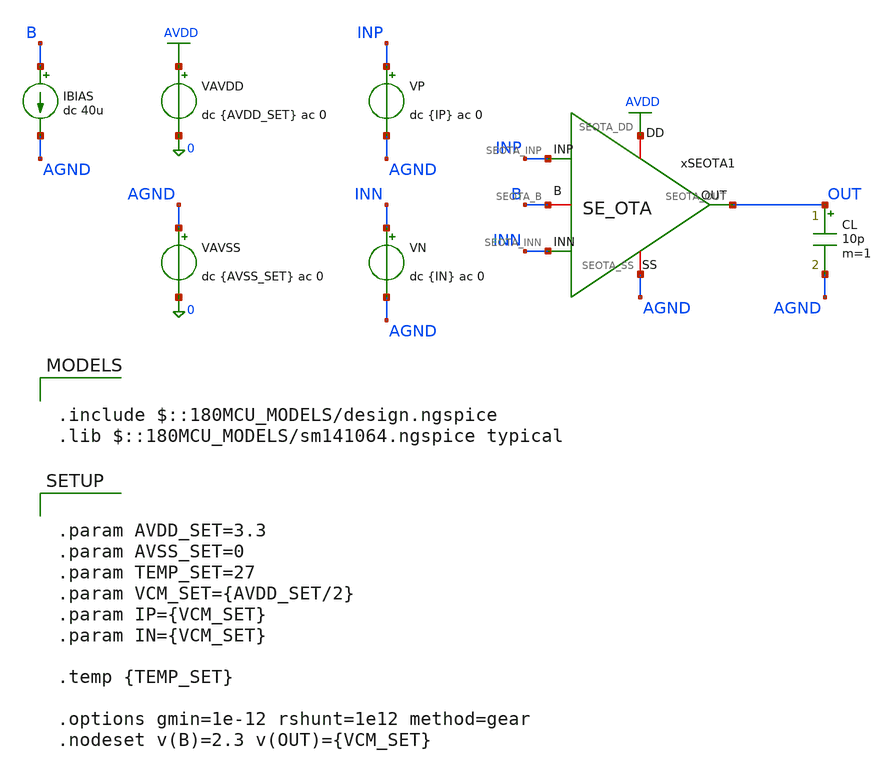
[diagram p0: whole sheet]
** sch_path: Design_Files/IC Design/Testbench/SE_OTA_OTA/Open_Loop_Noise/SE_OTA_TB_OL_NOISE_NOM.sch
**.subckt SE_OTA_TB_OL_NOISE_NOM
IBIAS B AGND dc 40u
VAVDD AVDD 0 dc {AVDD_SET} ac 0
.save i(vavdd)
CL OUT AGND 10p m=1
VP INP AGND dc {IP} ac 0
VN INN AGND dc {IN} ac 0
xSEOTA1 AVDD AGND INP INN OUT B SE_OTA
VAVSS AGND 0 dc {AVSS_SET} ac 0
.save i(vavss)
**** begin user architecture code

.include $::180MCU_MODELS/design.ngspice
.lib $::180MCU_MODELS/sm141064.ngspice typical



.control
destroy all
save all
set wr_singlescale

shell mkdir -p /foss/designs/ECG_Acquisition_IC/Measurement_Results/IC_Simulation/SE_OTA

let avdd_run = 3.3
let vcm_run  = avdd_run/2
let off_lo   = vcm_run - 0.05
let off_hi   = vcm_run + 0.05
let off_step = 10u

* OP
op
let op_avdd  = v(avdd) - v(agnd)
let op_inp   = v(inp)  - v(agnd)
let op_inn   = v(inn)  - v(agnd)
let op_out   = v(out)  - v(agnd)
let op_b     = v(b)    - v(agnd)
let op_idd   = -vavdd#branch
let op_ivss  =  vavss#branch
let op_ibias = 40e-6
wrdata /foss/designs/ECG_Acquisition_IC/Measurement_Results/IC_Simulation/SE_OTA/NOM.ol_op.txt
+ op_avdd op_inp op_inn op_out op_b op_idd op_ivss op_ibias

* Offset
dc VP $&off_lo $&off_hi $&off_step
let off_inp = v(inp) - v(agnd)
let off_inn = v(inn) - v(agnd)
let off_out = v(out) - v(agnd)
wrdata /foss/designs/ECG_Acquisition_IC/Measurement_Results/IC_Simulation/SE_OTA/NOM.ol_offset.txt
+ off_inp off_inn off_out

* Diff AC
alter @VP[DC] = $&vcm_run
alter @VN[DC] = $&vcm_run
alter @VP[ACMAG] = 0.5
alter @VP[ACPHASE] = 0
alter @VN[ACMAG] = 0.5
alter @VN[ACPHASE] = 180
alter @VAVDD[ACMAG] = 0
alter @VAVSS[ACMAG] = 0

ac dec 200 1 1G
let out_rel = v(out) - v(agnd)
wrdata /foss/designs/ECG_Acquisition_IC/Measurement_Results/IC_Simulation/SE_OTA/NOM.ol_ac_diff.txt
+ db(out_rel) ph(out_rel) mag(out_rel)

* CMRR
alter @VP[ACMAG] = 1
alter @VP[ACPHASE] = 0
alter @VN[ACMAG] = 1
alter @VN[ACPHASE] = 0
alter @VAVDD[ACMAG] = 0
alter @VAVSS[ACMAG] = 0

ac dec 200 1 1G
let out_rel = v(out) - v(agnd)
wrdata /foss/designs/ECG_Acquisition_IC/Measurement_Results/IC_Simulation/SE_OTA/NOM.ol_ac_cm.txt
+ db(out_rel) mag(out_rel)

* PSRR+
alter @VP[ACMAG] = 0
alter @VN[ACMAG] = 0
alter @VAVDD[ACMAG] = 1
alter @VAVDD[ACPHASE] = 0
alter @VAVSS[ACMAG] = 0

ac dec 200 1 1G
let out_rel = v(out) - v(agnd)
wrdata /foss/designs/ECG_Acquisition_IC/Measurement_Results/IC_Simulation/SE_OTA/NOM.ol_ac_psrrp.txt
+ db(out_rel) mag(out_rel)

* PSRR-
alter @VP[ACMAG] = 0
alter @VN[ACMAG] = 0
alter @VAVDD[ACMAG] = 0
alter @VAVSS[ACMAG] = 1
alter @VAVSS[ACPHASE] = 0

ac dec 200 1 1G
let out_rel = v(out) - v(agnd)
wrdata /foss/designs/ECG_Acquisition_IC/Measurement_Results/IC_Simulation/SE_OTA/NOM.ol_ac_psrrn.txt
+ db(out_rel) mag(out_rel)

* Noise total
alter @VAVDD[ACMAG] = 0
alter @VAVSS[ACMAG] = 0
alter @VP[ACMAG] = 1
alter @VN[ACMAG] = 0

noise v(OUT) VP dec 100 0.05 150
wrdata
+ /foss/designs/ECG_Acquisition_IC/Measurement_Results/IC_Simulation/SE_OTA/NOM.ol_noise_total.txt inoise_total onoise_total

* ICMR, 0.01 V step
alter @VP[ACMAG] = 0
alter @VN[ACMAG] = 0
alter @VAVDD[ACMAG] = 0
alter @VAVSS[ACMAG] = 0

dc VP 0 $&avdd_run 0.01 VN 0 $&avdd_run 0.01
let icmr_inp = v(inp) - v(agnd)
let icmr_inn = v(inn) - v(agnd)
let icmr_vcm = 0.5*(icmr_inp + icmr_inn)
let icmr_vid = icmr_inp - icmr_inn
let icmr_out = v(out) - v(agnd)
let icmr_idd = -vavdd#branch
let icmr_ivss = vavss#branch
wrdata /foss/designs/ECG_Acquisition_IC/Measurement_Results/IC_Simulation/SE_OTA/NOM.ol_icmr_dc.txt
+ icmr_vcm icmr_vid icmr_out icmr_idd icmr_ivss

* Differential input, 0.01 V step
alter @VN[DC] = $&vcm_run
dc VP 1.55 1.75 0.01
let diff_inp = v(inp) - v(agnd)
let diff_inn = v(inn) - v(agnd)
let diff_vid = diff_inp - diff_inn
let diff_vcm = 0.5*(diff_inp + diff_inn)
let diff_out = v(out) - v(agnd)
let diff_idd = -vavdd#branch
wrdata /foss/designs/ECG_Acquisition_IC/Measurement_Results/IC_Simulation/SE_OTA/NOM.ol_diff_dc.txt
+ diff_vid diff_vcm diff_out diff_idd

.endc




.param AVDD_SET=3.3
.param AVSS_SET=0
.param TEMP_SET=27
.param VCM_SET={AVDD_SET/2}
.param IP={VCM_SET}
.param IN={VCM_SET}

.temp {TEMP_SET}

.options gmin=1e-12 rshunt=1e12 method=gear
.nodeset v(B)=2.3 v(OUT)={VCM_SET}


**** end user architecture code
**.ends

* expanding   symbol:  ECG_Acquisition_IC/Design_Files/IC Design/Schematic/SE_OTA/SE_OTA.sym # of
*+ pins=6
** sym_path: Design_Files/IC Design/Schematic/SE_OTA/SE_OTA.sym
** sch_path: Design_Files/IC Design/Schematic/SE_OTA/SE_OTA.sch
.subckt SE_OTA SEOTA_DD SEOTA_SS SEOTA_INP SEOTA_INN SEOTA_OUT SEOTA_B
*.iopin SEOTA_DD
*.iopin SEOTA_SS
*.ipin SEOTA_INP
*.ipin SEOTA_INN
*.opin SEOTA_OUT
*.iopin SEOTA_B
XM4 net1 net4 SEOTA_SS SEOTA_SS nfet_03v3 L=2u W=2u nf=1 ad='int((nf+1)/2) * W/nf * 0.18u' as='int((nf+2)/2) * W/nf * 0.18u'
+ pd='2*int((nf+1)/2) * (W/nf + 0.18u)' ps='2*int((nf+2)/2) * (W/nf + 0.18u)' nrd='0.18u / W' nrs='0.18u / W'
+ sa=0 sb=0 sd=0 m=2
XM3 net4 net4 SEOTA_SS SEOTA_SS nfet_03v3 L=2u W=2u nf=1 ad='int((nf+1)/2) * W/nf * 0.18u' as='int((nf+2)/2) * W/nf * 0.18u'
+ pd='2*int((nf+1)/2) * (W/nf + 0.18u)' ps='2*int((nf+2)/2) * (W/nf + 0.18u)' nrd='0.18u / W' nrs='0.18u / W'
+ sa=0 sb=0 sd=0 m=2
XM1 net4 SEOTA_INN net3 SEOTA_DD pfet_03v3 L=1u W=32u nf=16 ad='int((nf+1)/2) * W/nf * 0.18u' as='int((nf+2)/2) * W/nf * 0.18u'
+ pd='2*int((nf+1)/2) * (W/nf + 0.18u)' ps='2*int((nf+2)/2) * (W/nf + 0.18u)' nrd='0.18u / W' nrs='0.18u / W'
+ sa=0 sb=0 sd=0 m=2
XM2 net1 SEOTA_INP net3 SEOTA_DD pfet_03v3 L=1u W=32u nf=16 ad='int((nf+1)/2) * W/nf * 0.18u' as='int((nf+2)/2) * W/nf * 0.18u'
+ pd='2*int((nf+1)/2) * (W/nf + 0.18u)' ps='2*int((nf+2)/2) * (W/nf + 0.18u)' nrd='0.18u / W' nrs='0.18u / W'
+ sa=0 sb=0 sd=0 m=2
XM7 SEOTA_OUT SEOTA_B SEOTA_DD SEOTA_DD pfet_03v3 L=0.5u W=56u nf=28 ad='int((nf+1)/2) * W/nf * 0.18u'
+ as='int((nf+2)/2) * W/nf * 0.18u' pd='2*int((nf+1)/2) * (W/nf + 0.18u)' ps='2*int((nf+2)/2) * (W/nf + 0.18u)'
+ nrd='0.18u / W' nrs='0.18u / W' sa=0 sb=0 sd=0 m=2
Rz net1 net2 0.5k m=1
XM5 net3 SEOTA_B SEOTA_DD SEOTA_DD pfet_03v3 L=2u W=20u nf=10 ad='int((nf+1)/2) * W/nf * 0.18u' as='int((nf+2)/2) * W/nf * 0.18u'
+ pd='2*int((nf+1)/2) * (W/nf + 0.18u)' ps='2*int((nf+2)/2) * (W/nf + 0.18u)' nrd='0.18u / W' nrs='0.18u / W'
+ sa=0 sb=0 sd=0 m=2
XM6 SEOTA_OUT net1 SEOTA_SS SEOTA_SS nfet_03v3 L=0.5u W=16u nf=8 ad='int((nf+1)/2) * W/nf * 0.18u' as='int((nf+2)/2) * W/nf * 0.18u'
+ pd='2*int((nf+1)/2) * (W/nf + 0.18u)' ps='2*int((nf+2)/2) * (W/nf + 0.18u)' nrd='0.18u / W' nrs='0.18u / W'
+ sa=0 sb=0 sd=0 m=2
XM8 SEOTA_B SEOTA_B SEOTA_DD SEOTA_DD pfet_03v3 L=2u W=50u nf=25 ad='int((nf+1)/2) * W/nf * 0.18u' as='int((nf+2)/2) * W/nf * 0.18u'
+ pd='2*int((nf+1)/2) * (W/nf + 0.18u)' ps='2*int((nf+2)/2) * (W/nf + 0.18u)' nrd='0.18u / W' nrs='0.18u / W'
+ sa=0 sb=0 sd=0 m=2
Cc net2 SEOTA_OUT 2p m=1
.ends

.GLOBAL AVDD
.end
